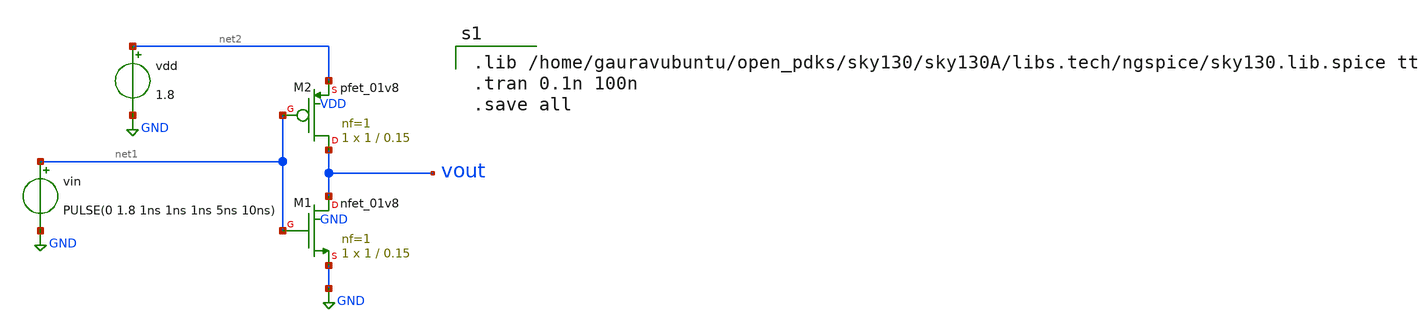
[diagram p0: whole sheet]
** sch_path: testInverter.sch
**.subckt testInverter
vin net1 GND PULSE(0 1.8 1ns 1ns 1ns 5ns 10ns)
vdd net2 GND 1.8
XM1 vout net1 GND GND sky130_fd_pr__nfet_01v8 L=0.15 W=1 nf=1 ad='int((1 + 1)/2) * 1 / 1 * 0.29' as='int((1 + 2)/2) * 1 / 1 * 0.29'
+ pd='2*int((1 + 1)/2) * (1 / 1 + 0.29)' ps='2*int((1 + 2)/2) * (1 / 1 + 0.29)' nrd='0.29 / 1 ' nrs='0.29 / 1 '
+ sa=0 sb=0 sd=0 mult=1 m=1
XM2 vout net1 net2 VDD sky130_fd_pr__pfet_01v8 L=0.15 W=1 nf=1 ad='int((1 + 1)/2) * 1 / 1 * 0.29' as='int((1 + 2)/2) * 1 / 1 * 0.29'
+ pd='2*int((1 + 1)/2) * (1 / 1 + 0.29)' ps='2*int((1 + 2)/2) * (1 / 1 + 0.29)' nrd='0.29 / 1 ' nrs='0.29 / 1 '
+ sa=0 sb=0 sd=0 mult=1 m=1
**** begin user architecture code

.lib /home/gauravubuntu/open_pdks/sky130/sky130A/libs.tech/ngspice/sky130.lib.spice tt
.tran 0.1n 100n
.save all

**** end user architecture code
**.ends
.GLOBAL GND
.end
